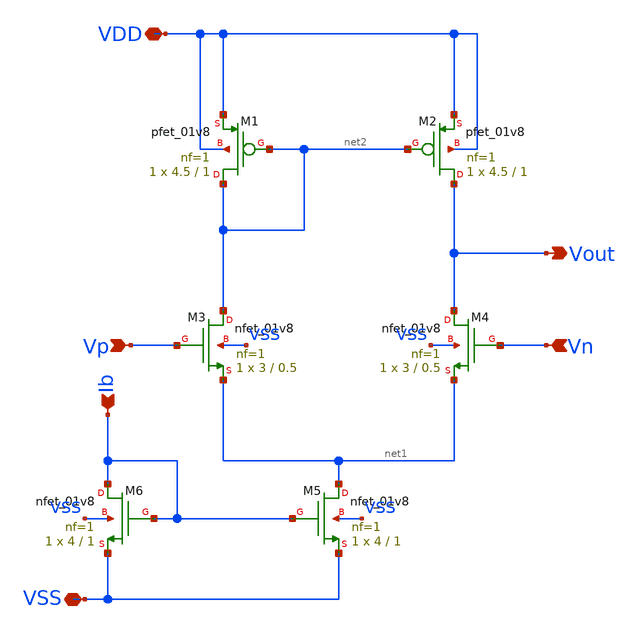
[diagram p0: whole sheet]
** sch_path: xschem/ota_5t.sch
**.subckt ota_5t VDD VSS Vout Vp Vn Ib
*.iopin VDD
*.iopin VSS
*.opin Vout
*.ipin Vp
*.ipin Vn
*.ipin Ib
XM3 net2 Vp net1 VSS sky130_fd_pr__nfet_01v8 L=0.5 W=3 nf=1 ad='int((1 + 1)/2) * 3 / 1 * 0.29' as='int((1 + 2)/2) * 3 / 1 * 0.29'
+ pd='2*int((1 + 1)/2) * (3 / 1 + 0.29)' ps='2*int((1 + 2)/2) * (3 / 1 + 0.29)' nrd='0.29 / 3 ' nrs='0.29 / 3 '
+ sa=0 sb=0 sd=0 mult=1 m=1
XM1 net2 net2 VDD VDD sky130_fd_pr__pfet_01v8 L=1 W=4.5 nf=1 ad='int((nf+1)/2) * W/nf * 0.29' as='int((nf+2)/2) * W/nf * 0.29'
+ pd='2*int((nf+1)/2) * (W/nf + 0.29)' ps='2*int((nf+2)/2) * (W/nf + 0.29)' nrd='0.29 / W' nrs='0.29 / W'
+ sa=0 sb=0 sd=0 mult=1 m=1
XM2 Vout net2 VDD VDD sky130_fd_pr__pfet_01v8 L=1 W=4.5 nf=1 ad='int((nf+1)/2) * W/nf * 0.29' as='int((nf+2)/2) * W/nf * 0.29'
+ pd='2*int((nf+1)/2) * (W/nf + 0.29)' ps='2*int((nf+2)/2) * (W/nf + 0.29)' nrd='0.29 / W' nrs='0.29 / W'
+ sa=0 sb=0 sd=0 mult=1 m=1
XM4 Vout Vn net1 VSS sky130_fd_pr__nfet_01v8 L=0.5 W=3 nf=1 ad='int((1 + 1)/2) * 3 / 1 * 0.29' as='int((1 + 2)/2) * 3 / 1 * 0.29'
+ pd='2*int((1 + 1)/2) * (3 / 1 + 0.29)' ps='2*int((1 + 2)/2) * (3 / 1 + 0.29)' nrd='0.29 / 3 ' nrs='0.29 / 3 '
+ sa=0 sb=0 sd=0 mult=1 m=1
XM5 net1 Ib VSS VSS sky130_fd_pr__nfet_01v8 L=1 W=4 nf=1 ad='int((1 + 1)/2) * 4 / 1 * 0.29' as='int((1 + 2)/2) * 4 / 1 * 0.29'
+ pd='2*int((1 + 1)/2) * (4 / 1 + 0.29)' ps='2*int((1 + 2)/2) * (4 / 1 + 0.29)' nrd='0.29 / 4 ' nrs='0.29 / 4 '
+ sa=0 sb=0 sd=0 mult=1 m=1
XM6 Ib Ib VSS VSS sky130_fd_pr__nfet_01v8 L=1 W=4 nf=1 ad='int((1 + 1)/2) * 4 / 1 * 0.29' as='int((1 + 2)/2) * 4 / 1 * 0.29'
+ pd='2*int((1 + 1)/2) * (4 / 1 + 0.29)' ps='2*int((1 + 2)/2) * (4 / 1 + 0.29)' nrd='0.29 / 4 ' nrs='0.29 / 4 '
+ sa=0 sb=0 sd=0 mult=1 m=1
**.ends
.end
